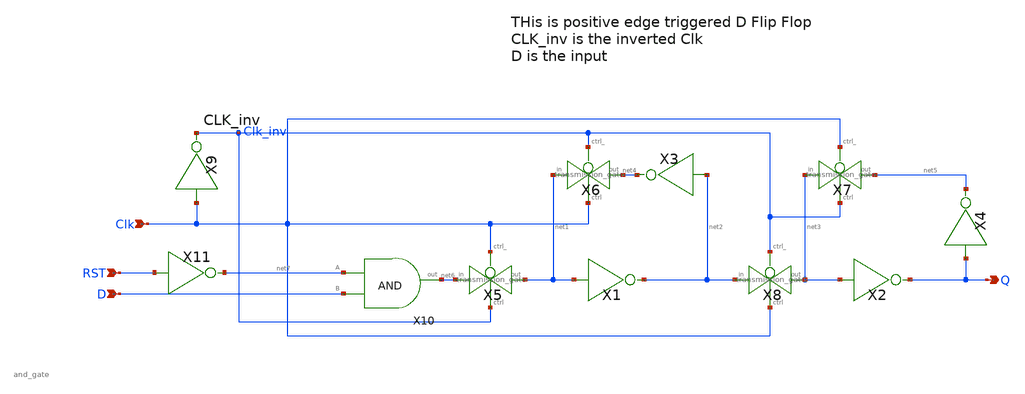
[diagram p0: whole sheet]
** sch_path: xschem/D_flip_flop/d_ff_rst.sch
**.subckt d_ff_rst D Clk Q RST
*.ipin D
*.ipin Clk
*.opin Q
*.ipin RST
X1 net1 net2 inv
X2 net3 Q inv
X3 net2 net4 inv
X4 Q net5 inv
X5 net6 net1 Clk Clk_inv transmission_gate
X6 net1 net4 Clk_inv Clk transmission_gate
X7 net3 net5 Clk Clk_inv transmission_gate
X8 net2 net3 Clk_inv Clk transmission_gate
X9 Clk Clk_inv inv
X10 net7 D net6 and_gate
X11 RST net7 inv
**.ends

* expanding   symbol:  inv/inv.sym # of pins=2
** sym_path: xschem/inv/inv.sym
** sch_path: xschem/inv/inv.sch
.subckt inv in out
*.ipin in
*.iopin out
XM1 out in GND GND sky130_fd_pr__nfet_01v8 L=0.18 W=1 nf=1 ad='int((nf+1)/2) * W/nf * 0.29' as='int((nf+2)/2) * W/nf * 0.29'
+ pd='2*int((nf+1)/2) * (W/nf + 0.29)' ps='2*int((nf+2)/2) * (W/nf + 0.29)' nrd='0.29 / W' nrs='0.29 / W'
+ sa=0 sb=0 sd=0 mult=1 m=1
XM2 out in VDD VDD sky130_fd_pr__pfet_01v8 L=0.18 W=3 nf=1 ad='int((nf+1)/2) * W/nf * 0.29' as='int((nf+2)/2) * W/nf * 0.29'
+ pd='2*int((nf+1)/2) * (W/nf + 0.29)' ps='2*int((nf+2)/2) * (W/nf + 0.29)' nrd='0.29 / W' nrs='0.29 / W'
+ sa=0 sb=0 sd=0 mult=1 m=1
.ends


* expanding   symbol:  transmission_gate/transmission_gate.sym # of pins=4
** sym_path: xschem/transmission_gate/transmission_gate.sym
** sch_path: xschem/transmission_gate/transmission_gate.sch
.subckt transmission_gate in out ctrl_ ctrl
*.iopin in
*.iopin out
*.ipin ctrl_
*.ipin ctrl
XM3 in ctrl out GND sky130_fd_pr__nfet_01v8 L=0.18 W=1 nf=1 ad='int((nf+1)/2) * W/nf * 0.29' as='int((nf+2)/2) * W/nf * 0.29'
+ pd='2*int((nf+1)/2) * (W/nf + 0.29)' ps='2*int((nf+2)/2) * (W/nf + 0.29)' nrd='0.29 / W' nrs='0.29 / W'
+ sa=0 sb=0 sd=0 mult=1 m=1
XM4 out ctrl_ in VDD sky130_fd_pr__pfet_01v8 L=0.18 W=1 nf=1 ad='int((nf+1)/2) * W/nf * 0.29' as='int((nf+2)/2) * W/nf * 0.29'
+ pd='2*int((nf+1)/2) * (W/nf + 0.29)' ps='2*int((nf+2)/2) * (W/nf + 0.29)' nrd='0.29 / W' nrs='0.29 / W'
+ sa=0 sb=0 sd=0 mult=1 m=1
.ends


* expanding   symbol:  and_gate/and_gate.sym # of pins=3
** sym_path: and_gate/and_gate.sym
** sch_path: and_gate/and_gate.sch
.subckt and_gate A B out
*.ipin A
*.ipin B
*.opin out
XM1 net1 A net2 GND sky130_fd_pr__nfet_01v8 L=0.18 W=2 nf=1 ad='int((nf+1)/2) * W/nf * 0.29' as='int((nf+2)/2) * W/nf * 0.29'
+ pd='2*int((nf+1)/2) * (W/nf + 0.29)' ps='2*int((nf+2)/2) * (W/nf + 0.29)' nrd='0.29 / W' nrs='0.29 / W'
+ sa=0 sb=0 sd=0 mult=1 m=1
XM2 net1 A VDD VDD sky130_fd_pr__pfet_01v8 L=0.18 W=2 nf=1 ad='int((nf+1)/2) * W/nf * 0.29' as='int((nf+2)/2) * W/nf * 0.29'
+ pd='2*int((nf+1)/2) * (W/nf + 0.29)' ps='2*int((nf+2)/2) * (W/nf + 0.29)' nrd='0.29 / W' nrs='0.29 / W'
+ sa=0 sb=0 sd=0 mult=1 m=1
XM3 net1 B VDD VDD sky130_fd_pr__pfet_01v8 L=0.18 W=2 nf=1 ad='int((nf+1)/2) * W/nf * 0.29' as='int((nf+2)/2) * W/nf * 0.29'
+ pd='2*int((nf+1)/2) * (W/nf + 0.29)' ps='2*int((nf+2)/2) * (W/nf + 0.29)' nrd='0.29 / W' nrs='0.29 / W'
+ sa=0 sb=0 sd=0 mult=1 m=1
XM4 net2 B GND GND sky130_fd_pr__nfet_01v8 L=0.18 W=2 nf=1 ad='int((nf+1)/2) * W/nf * 0.29' as='int((nf+2)/2) * W/nf * 0.29'
+ pd='2*int((nf+1)/2) * (W/nf + 0.29)' ps='2*int((nf+2)/2) * (W/nf + 0.29)' nrd='0.29 / W' nrs='0.29 / W'
+ sa=0 sb=0 sd=0 mult=1 m=1
X1 net1 out inv
.ends

.GLOBAL VDD
.GLOBAL GND
.end
